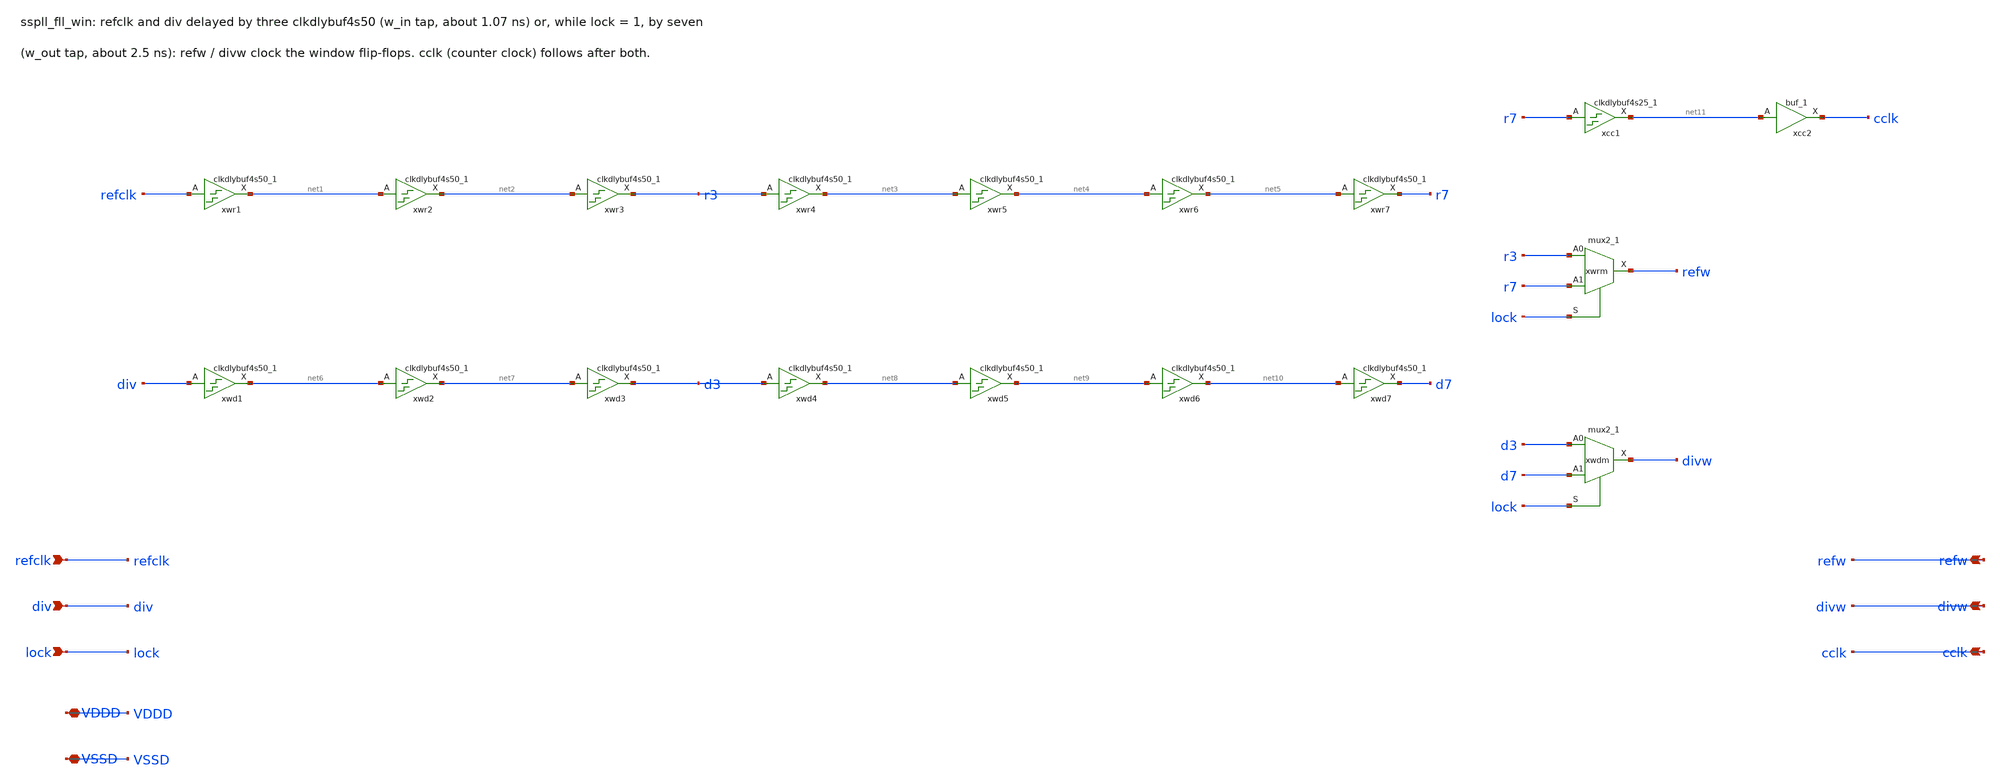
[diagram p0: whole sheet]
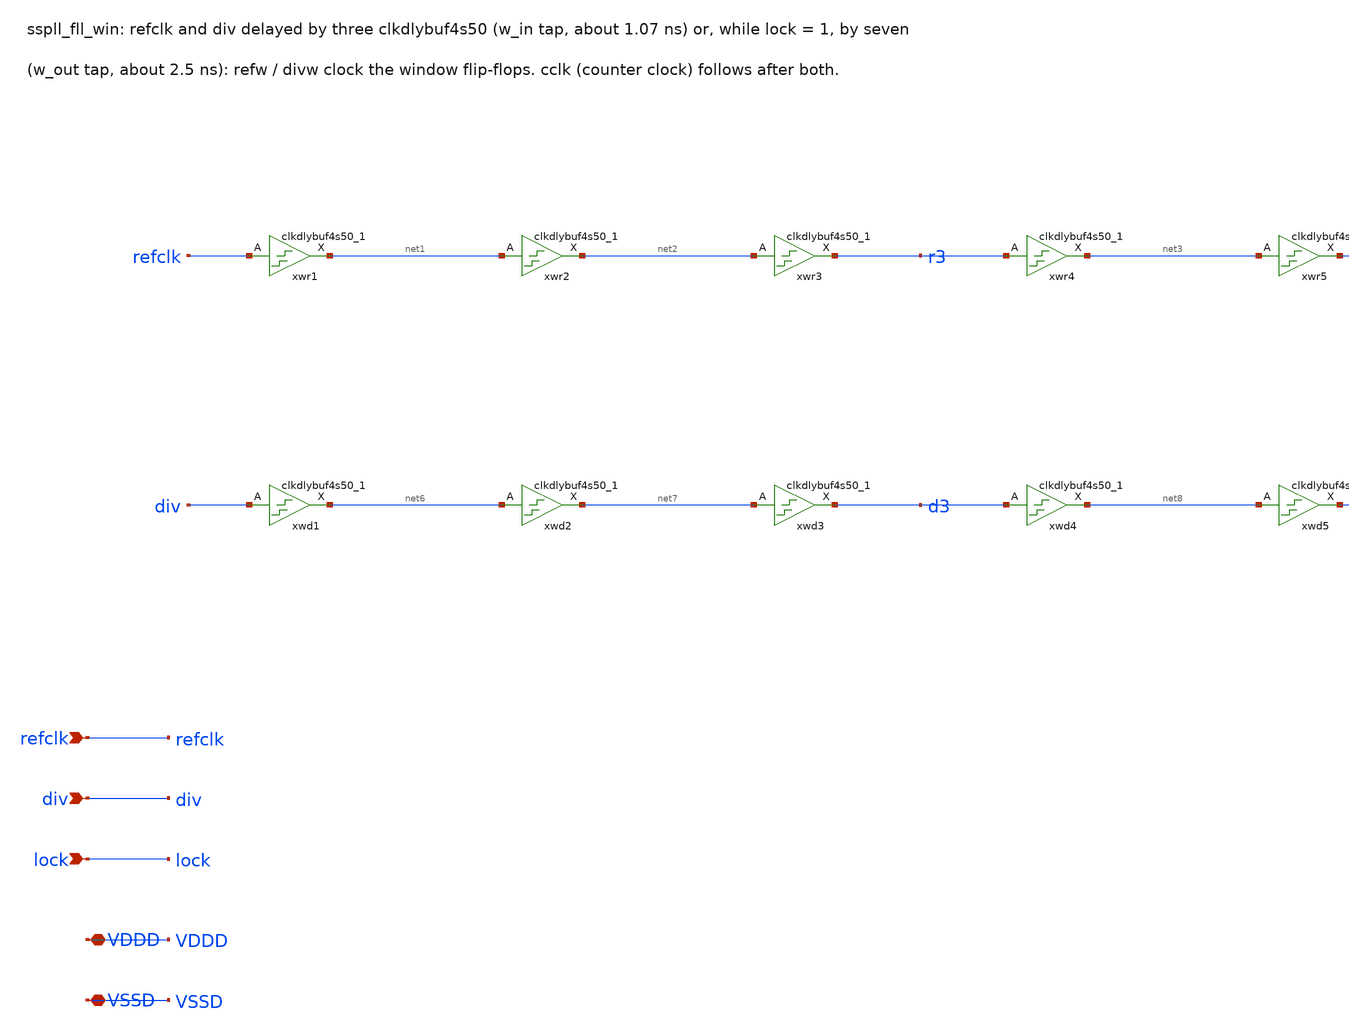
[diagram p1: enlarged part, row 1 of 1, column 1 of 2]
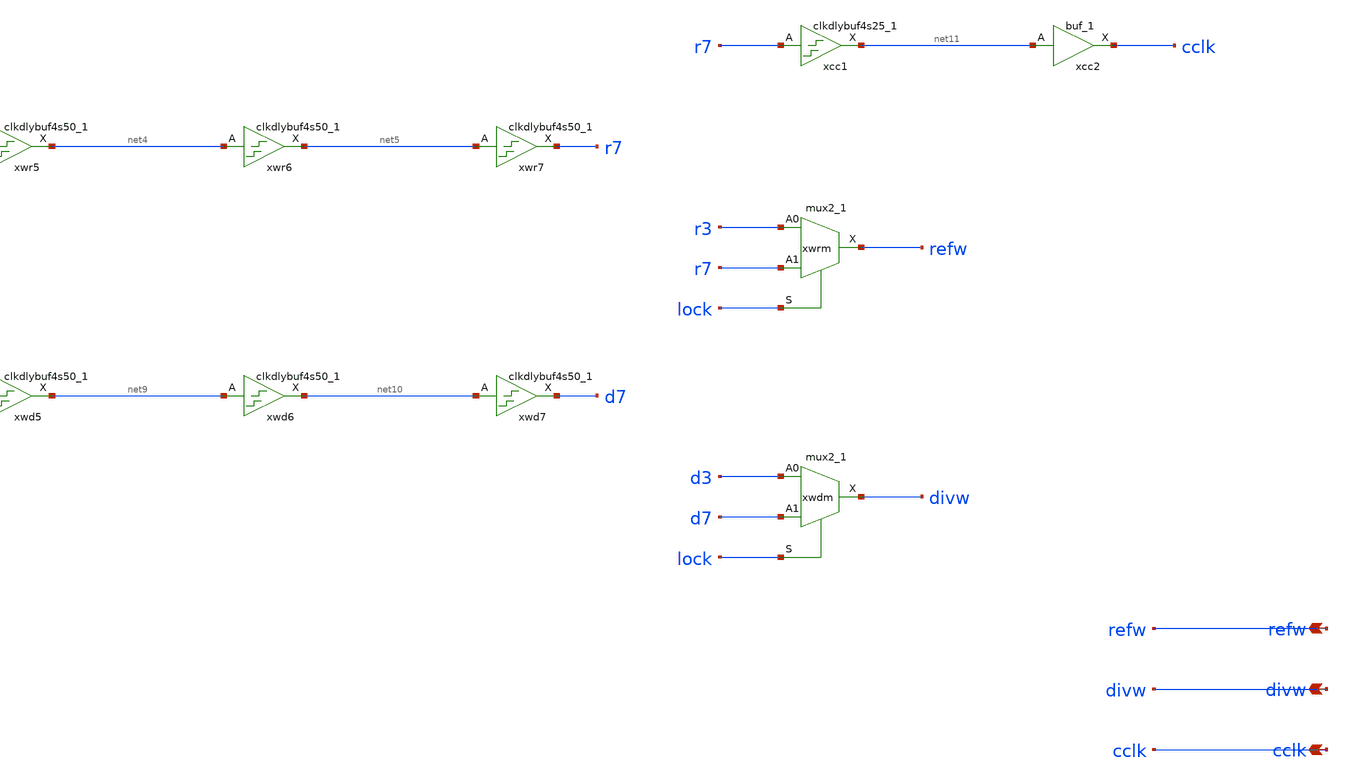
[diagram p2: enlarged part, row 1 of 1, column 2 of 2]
** sch_path: xschem/fll_hv/sspll_fll_win.sch
**.subckt sspll_fll_win refclk div lock refw divw cclk VDDD VSSD
*.ipin refclk
*.ipin div
*.ipin lock
*.opin refw
*.opin divw
*.opin cclk
*.iopin VDDD
*.iopin VSSD
xwr1 refclk VSSD VSSD VDDD VDDD net1 sky130_fd_sc_hd__clkdlybuf4s50_1
xwr2 net1 VSSD VSSD VDDD VDDD net2 sky130_fd_sc_hd__clkdlybuf4s50_1
xwr3 net2 VSSD VSSD VDDD VDDD r3 sky130_fd_sc_hd__clkdlybuf4s50_1
xwr4 r3 VSSD VSSD VDDD VDDD net3 sky130_fd_sc_hd__clkdlybuf4s50_1
xwr5 net3 VSSD VSSD VDDD VDDD net4 sky130_fd_sc_hd__clkdlybuf4s50_1
xwr6 net4 VSSD VSSD VDDD VDDD net5 sky130_fd_sc_hd__clkdlybuf4s50_1
xwr7 net5 VSSD VSSD VDDD VDDD r7 sky130_fd_sc_hd__clkdlybuf4s50_1
xwrm r3 r7 lock VSSD VSSD VDDD VDDD refw sky130_fd_sc_hd__mux2_1
xwd1 div VSSD VSSD VDDD VDDD net6 sky130_fd_sc_hd__clkdlybuf4s50_1
xwd2 net6 VSSD VSSD VDDD VDDD net7 sky130_fd_sc_hd__clkdlybuf4s50_1
xwd3 net7 VSSD VSSD VDDD VDDD d3 sky130_fd_sc_hd__clkdlybuf4s50_1
xwd4 d3 VSSD VSSD VDDD VDDD net8 sky130_fd_sc_hd__clkdlybuf4s50_1
xwd5 net8 VSSD VSSD VDDD VDDD net9 sky130_fd_sc_hd__clkdlybuf4s50_1
xwd6 net9 VSSD VSSD VDDD VDDD net10 sky130_fd_sc_hd__clkdlybuf4s50_1
xwd7 net10 VSSD VSSD VDDD VDDD d7 sky130_fd_sc_hd__clkdlybuf4s50_1
xwdm d3 d7 lock VSSD VSSD VDDD VDDD divw sky130_fd_sc_hd__mux2_1
xcc1 r7 VSSD VSSD VDDD VDDD net11 sky130_fd_sc_hd__clkdlybuf4s25_1
xcc2 net11 VSSD VSSD VDDD VDDD cclk sky130_fd_sc_hd__buf_1
**.ends
.end
